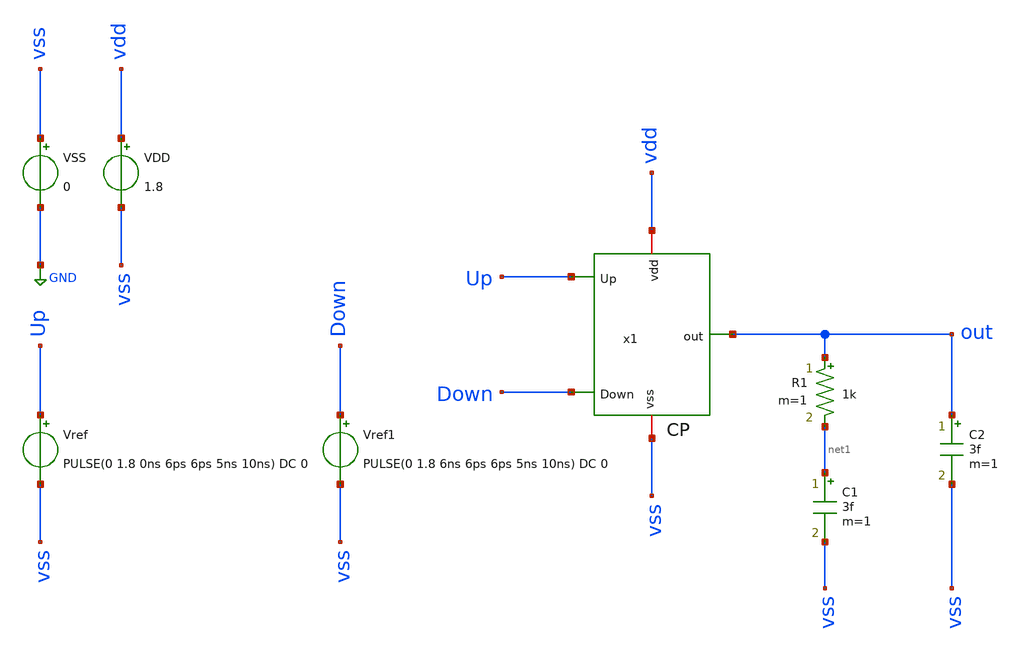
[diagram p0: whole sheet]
** sch_path: sch/PLL_caravel/tb_CP.sch
**.subckt tb_CP
VSS vss GND 0
VDD vdd vss 1.8
Vref Up vss PULSE(0 1.8 0ns 6ps 6ps 5ns 10ns) DC 0
Vref1 Down vss PULSE(0 1.8 6ns 6ps 6ps 5ns 10ns) DC 0
C1 net1 vss 3f m=1
x1 vdd Down out Up vss CP
R1 out net1 1k m=1
C2 out vss 3f m=1
**** begin user architecture code



* Parameters
.options TEMPS = 27.0

* Models
.lib ~/skywater/skywater-pdk/libraries/sky130_fd_pr_ngspice/latest/models/corners/sky130.lib TT

* Data to save
.save all



* Simulation
.ic v(out) = 0
*.ic i(out) = 0
.control
	tran 10n 300ns
        setplot tran1
        plot v(Up)+12 v(Down)+8 v(out)+4 C(out)
        set filetype = ascii
        write CP_tran.raw
.endc

.end


**** end user architecture code
**.ends

* expanding   symbol:  PLL_caravel/CP.sym # of pins=5
** sym_path: sch/PLL_caravel/CP.sym
** sch_path: sch/PLL_caravel/CP.sch
.subckt CP vdd Down out Up vss
*.iopin vdd
*.ipin Down
*.opin out
*.iopin vss
*.ipin Up
XM1 outP net1 vdd vdd sky130_fd_pr__pfet_01v8 L=0.15 W=5.4 nf=1 ad='int((nf+1)/2) * W/nf * 0.29' as='int((nf+2)/2) * W/nf * 0.29'
+ pd='2*int((nf+1)/2) * (W/nf + 0.29)' ps='2*int((nf+2)/2) * (W/nf + 0.29)' nrd='0.29 / W' nrs='0.29 / W'
+ sa=0 sb=0 sd=0 mult=1 m=1
XM2 out Up outN vss sky130_fd_pr__nfet_01v8 L=0.15 W=0.42 nf=1 ad='int((nf+1)/2) * W/nf * 0.29' as='int((nf+2)/2) * W/nf * 0.29'
+ pd='2*int((nf+1)/2) * (W/nf + 0.29)' ps='2*int((nf+2)/2) * (W/nf + 0.29)' nrd='0.29 / W' nrs='0.29 / W'
+ sa=0 sb=0 sd=0 mult=1 m=1
XM3 net1 net1 vdd vdd sky130_fd_pr__pfet_01v8 L=0.15 W=0.42 nf=1 ad='int((nf+1)/2) * W/nf * 0.29' as='int((nf+2)/2) * W/nf * 0.29'
+ pd='2*int((nf+1)/2) * (W/nf + 0.29)' ps='2*int((nf+2)/2) * (W/nf + 0.29)' nrd='0.29 / W' nrs='0.29 / W'
+ sa=0 sb=0 sd=0 mult=1 m=1
XM4 out DownB outP vdd sky130_fd_pr__pfet_01v8 L=0.15 W=0.42 nf=1 ad='int((nf+1)/2) * W/nf * 0.29' as='int((nf+2)/2) * W/nf * 0.29'
+ pd='2*int((nf+1)/2) * (W/nf + 0.29)' ps='2*int((nf+2)/2) * (W/nf + 0.29)' nrd='0.29 / W' nrs='0.29 / W'
+ sa=0 sb=0 sd=0 mult=1 m=1
XM5 outN net2 vss vss sky130_fd_pr__nfet_01v8 L=0.15 W=5.4 nf=1 ad='int((nf+1)/2) * W/nf * 0.29' as='int((nf+2)/2) * W/nf * 0.29'
+ pd='2*int((nf+1)/2) * (W/nf + 0.29)' ps='2*int((nf+2)/2) * (W/nf + 0.29)' nrd='0.29 / W' nrs='0.29 / W'
+ sa=0 sb=0 sd=0 mult=1 m=1
XM6 net2 net2 vss vss sky130_fd_pr__nfet_01v8 L=0.15 W=0.42 nf=1 ad='int((nf+1)/2) * W/nf * 0.29' as='int((nf+2)/2) * W/nf * 0.29'
+ pd='2*int((nf+1)/2) * (W/nf + 0.29)' ps='2*int((nf+2)/2) * (W/nf + 0.29)' nrd='0.29 / W' nrs='0.29 / W'
+ sa=0 sb=0 sd=0 mult=1 m=1
XM7 net3 Down outP vdd sky130_fd_pr__pfet_01v8 L=0.15 W=5.4 nf=1 ad='int((nf+1)/2) * W/nf * 0.29' as='int((nf+2)/2) * W/nf * 0.29'
+ pd='2*int((nf+1)/2) * (W/nf + 0.29)' ps='2*int((nf+2)/2) * (W/nf + 0.29)' nrd='0.29 / W' nrs='0.29 / W'
+ sa=0 sb=0 sd=0 mult=1 m=1
XM8 net3 net3 vss vss sky130_fd_pr__nfet_01v8 L=0.15 W=0.42 nf=1 ad='int((nf+1)/2) * W/nf * 0.29' as='int((nf+2)/2) * W/nf * 0.29'
+ pd='2*int((nf+1)/2) * (W/nf + 0.29)' ps='2*int((nf+2)/2) * (W/nf + 0.29)' nrd='0.29 / W' nrs='0.29 / W'
+ sa=0 sb=0 sd=0 mult=1 m=1
XM9 net4 UpB outN vss sky130_fd_pr__nfet_01v8 L=0.15 W=5.4 nf=1 ad='int((nf+1)/2) * W/nf * 0.29' as='int((nf+2)/2) * W/nf * 0.29'
+ pd='2*int((nf+1)/2) * (W/nf + 0.29)' ps='2*int((nf+2)/2) * (W/nf + 0.29)' nrd='0.29 / W' nrs='0.29 / W'
+ sa=0 sb=0 sd=0 mult=1 m=1
XM10 net4 net4 vdd vdd sky130_fd_pr__pfet_01v8 L=0.15 W=0.42 nf=1 ad='int((nf+1)/2) * W/nf * 0.29' as='int((nf+2)/2) * W/nf * 0.29'
+ pd='2*int((nf+1)/2) * (W/nf + 0.29)' ps='2*int((nf+2)/2) * (W/nf + 0.29)' nrd='0.29 / W' nrs='0.29 / W'
+ sa=0 sb=0 sd=0 mult=1 m=1
XM11 DownB Down vdd vdd sky130_fd_pr__pfet_01v8 L=0.15 W=0.84 nf=1 ad='int((nf+1)/2) * W/nf * 0.29' as='int((nf+2)/2) * W/nf * 0.29'
+ pd='2*int((nf+1)/2) * (W/nf + 0.29)' ps='2*int((nf+2)/2) * (W/nf + 0.29)' nrd='0.29 / W' nrs='0.29 / W'
+ sa=0 sb=0 sd=0 mult=1 m=1
XM12 DownB Down vss vss sky130_fd_pr__nfet_01v8 L=0.15 W=0.42 nf=1 ad='int((nf+1)/2) * W/nf * 0.29' as='int((nf+2)/2) * W/nf * 0.29'
+ pd='2*int((nf+1)/2) * (W/nf + 0.29)' ps='2*int((nf+2)/2) * (W/nf + 0.29)' nrd='0.29 / W' nrs='0.29 / W'
+ sa=0 sb=0 sd=0 mult=1 m=1
XM13 UpB Up vdd vdd sky130_fd_pr__pfet_01v8 L=0.15 W=0.84 nf=1 ad='int((nf+1)/2) * W/nf * 0.29' as='int((nf+2)/2) * W/nf * 0.29'
+ pd='2*int((nf+1)/2) * (W/nf + 0.29)' ps='2*int((nf+2)/2) * (W/nf + 0.29)' nrd='0.29 / W' nrs='0.29 / W'
+ sa=0 sb=0 sd=0 mult=1 m=1
XM14 UpB Up vss vss sky130_fd_pr__nfet_01v8 L=0.15 W=0.42 nf=1 ad='int((nf+1)/2) * W/nf * 0.29' as='int((nf+2)/2) * W/nf * 0.29'
+ pd='2*int((nf+1)/2) * (W/nf + 0.29)' ps='2*int((nf+2)/2) * (W/nf + 0.29)' nrd='0.29 / W' nrs='0.29 / W'
+ sa=0 sb=0 sd=0 mult=1 m=1
.ends

.GLOBAL GND
.end
